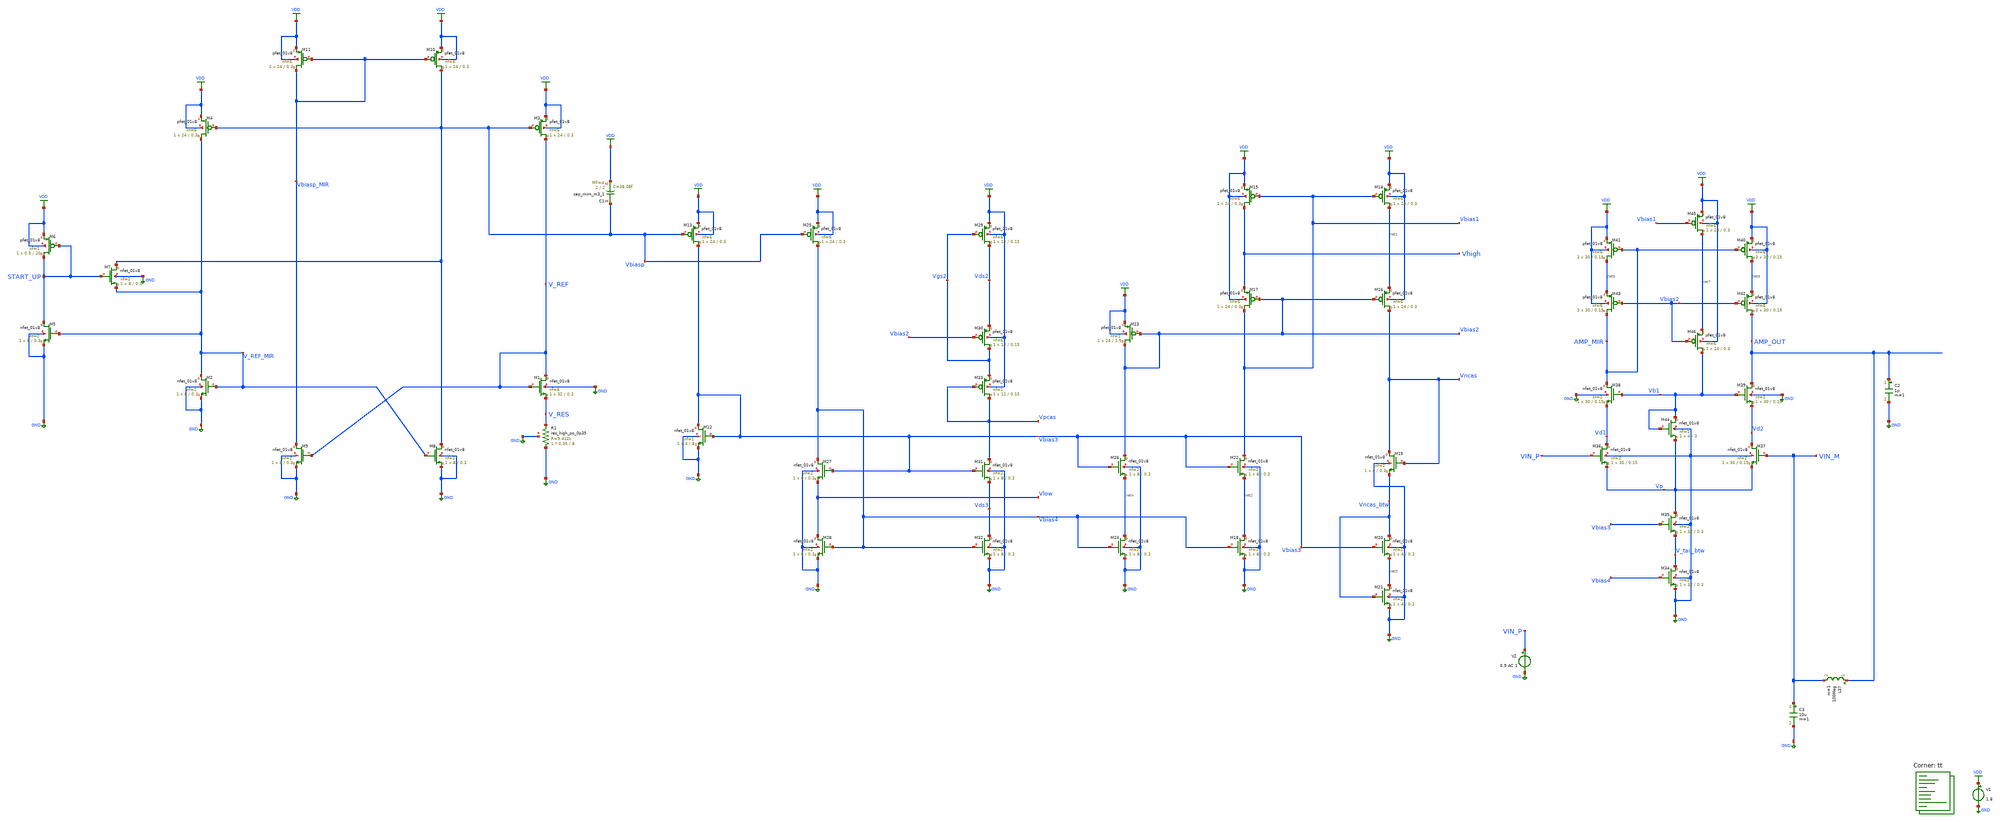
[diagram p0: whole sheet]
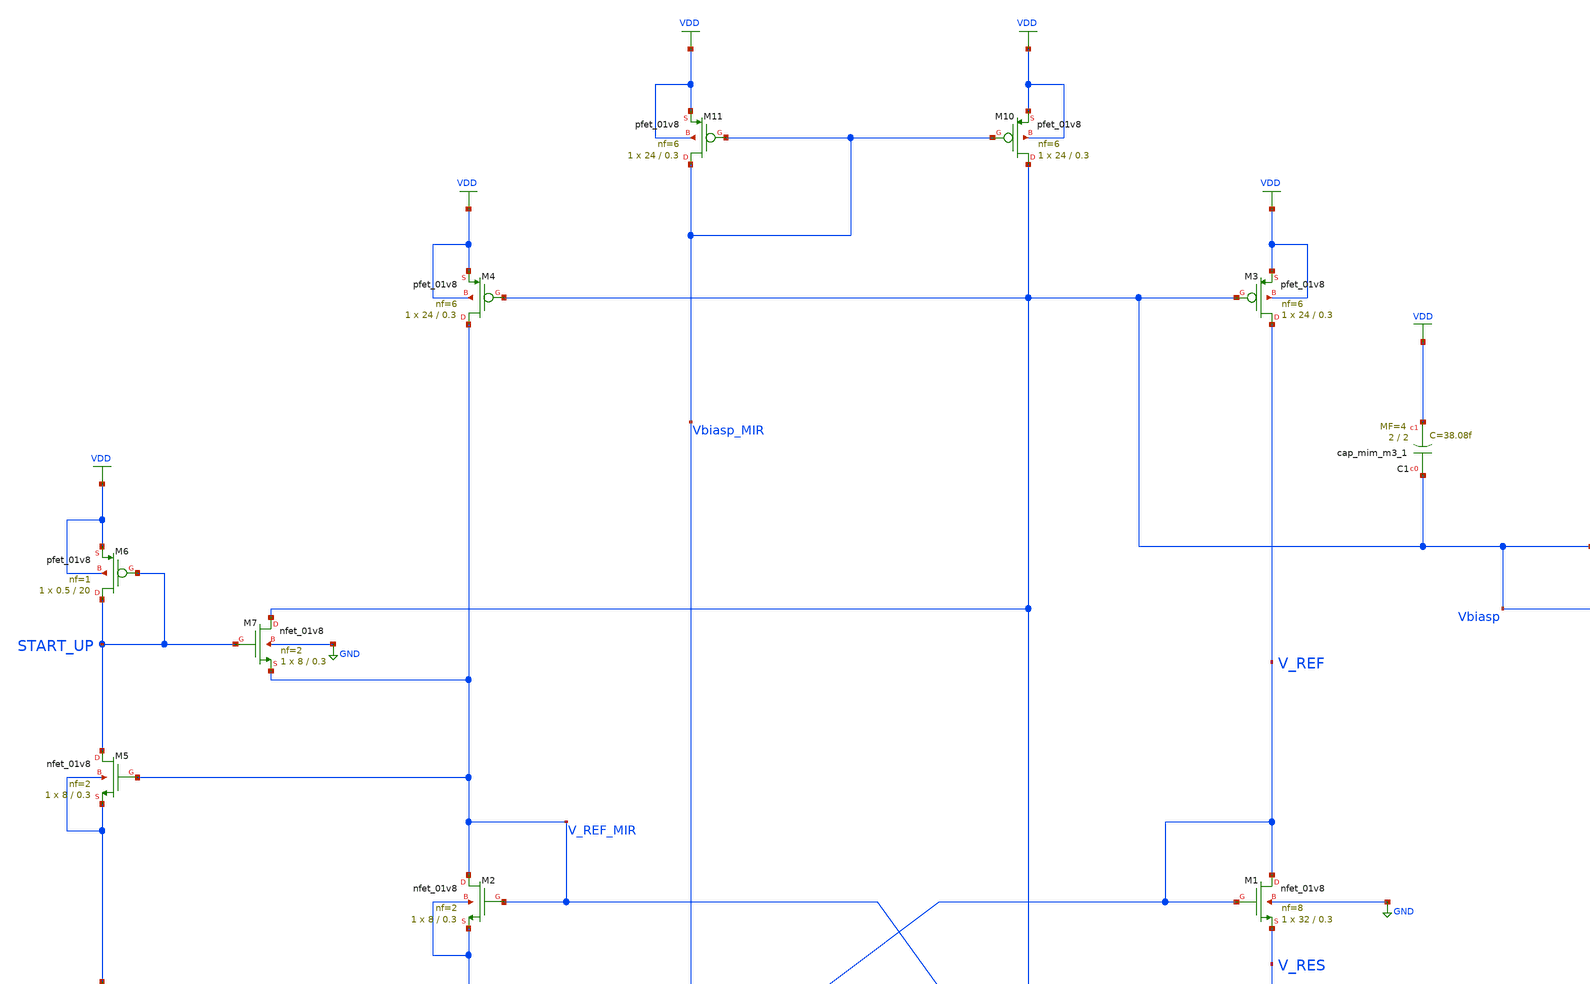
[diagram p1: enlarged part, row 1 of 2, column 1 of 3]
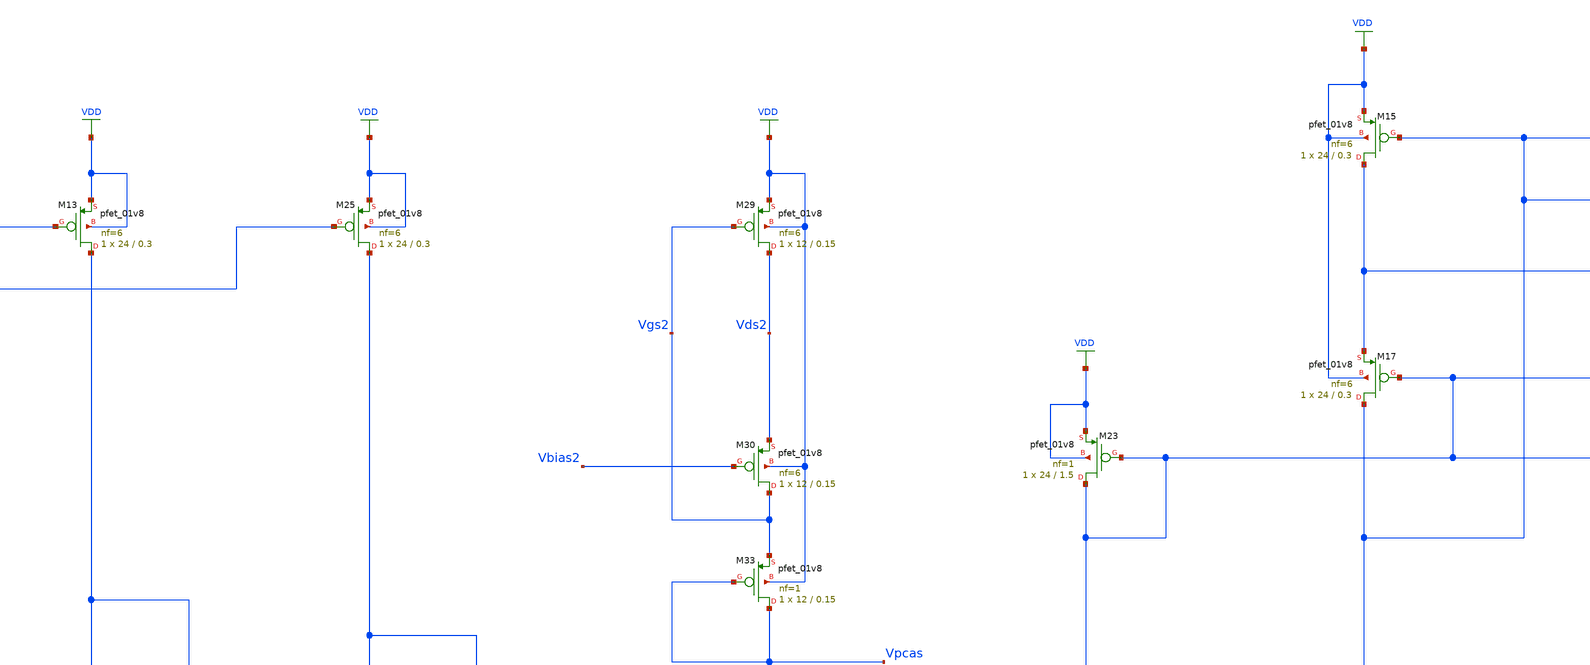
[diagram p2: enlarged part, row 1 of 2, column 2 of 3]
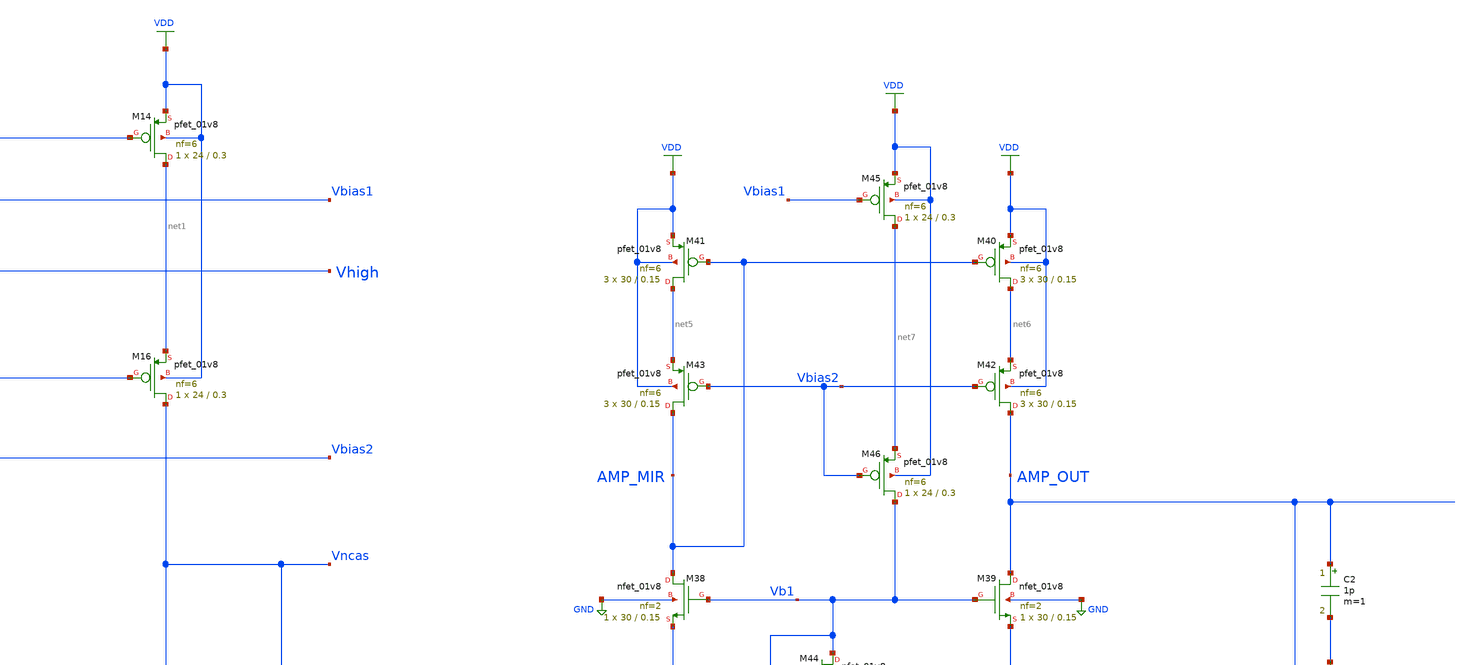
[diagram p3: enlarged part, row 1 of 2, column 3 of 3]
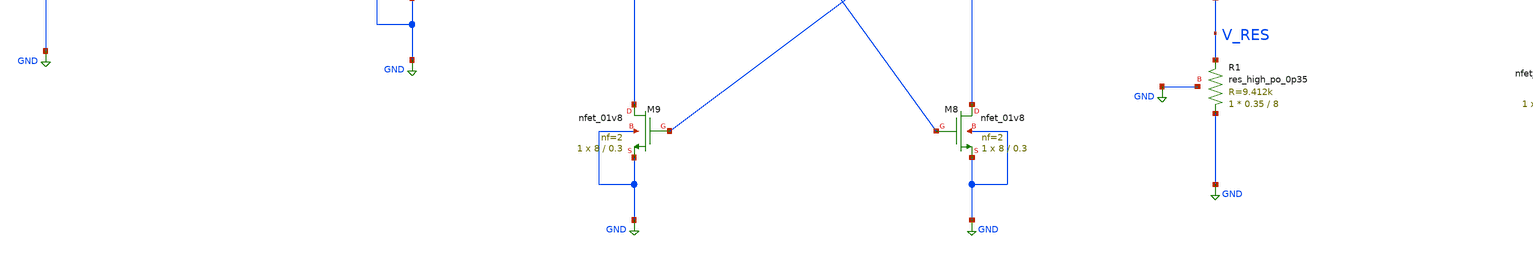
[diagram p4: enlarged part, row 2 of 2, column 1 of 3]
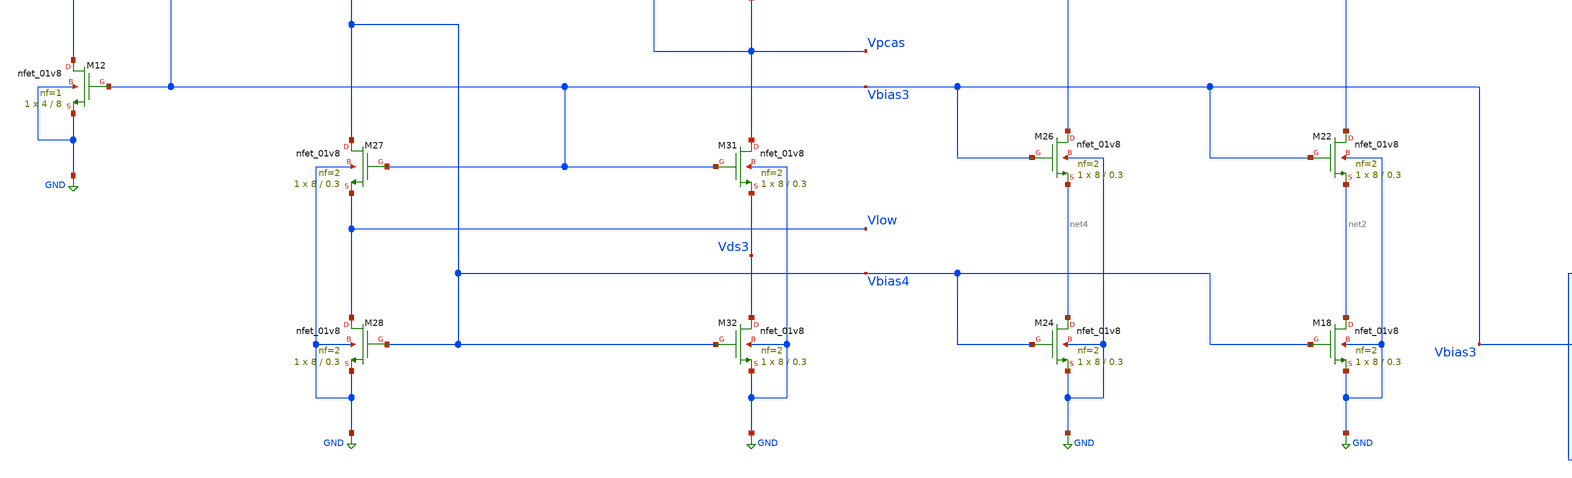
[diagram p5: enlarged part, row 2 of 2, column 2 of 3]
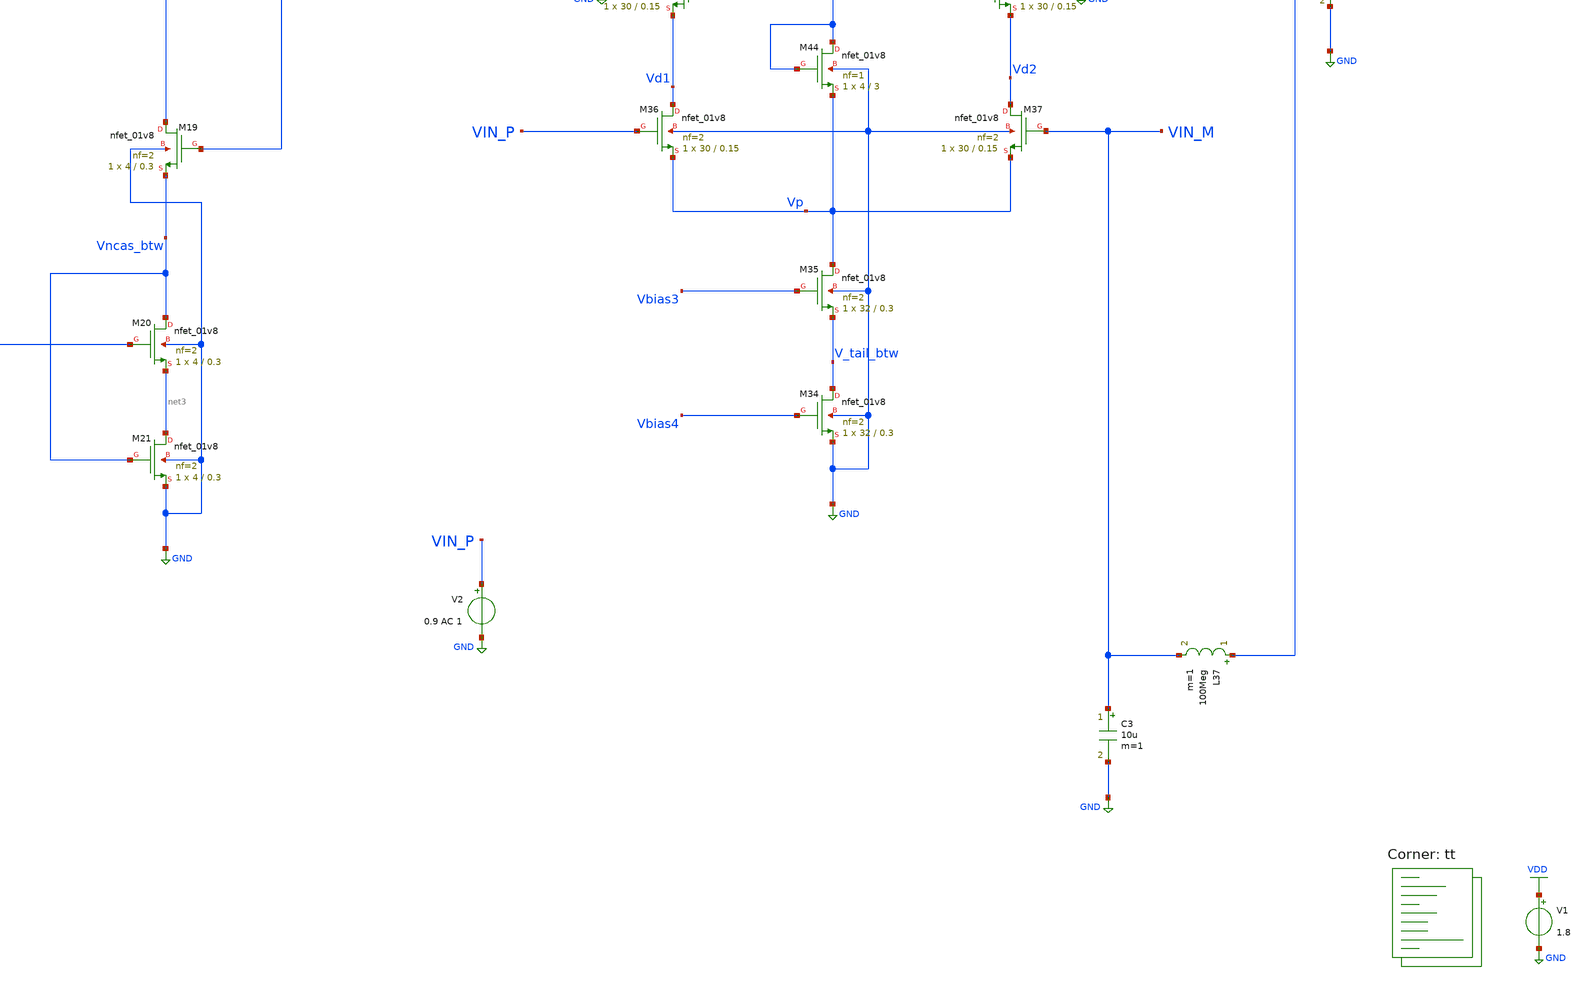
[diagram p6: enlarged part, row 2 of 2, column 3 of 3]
** sch_path: projects/ASU/EEE572/schematic/tb_tele_casc_diff_amp_AC.sch
**.subckt tb_tele_casc_diff_amp_AC
V1 VDD GND 1.8
XM1 V_REF V_REF V_RES GND sky130_fd_pr__nfet_01v8 L=0.3 W=32 nf=8 ad='int((nf+1)/2) * W/nf * 0.29' as='int((nf+2)/2) * W/nf * 0.29'
+ pd='2*int((nf+1)/2) * (W/nf + 0.29)' ps='2*int((nf+2)/2) * (W/nf + 0.29)' nrd='0.29 / W' nrs='0.29 / W'
+ sa=0 sb=0 sd=0 mult=1 m=1
XM2 V_REF_MIR V_REF_MIR GND GND sky130_fd_pr__nfet_01v8 L=0.3 W=8 nf=2 ad='int((nf+1)/2) * W/nf * 0.29'
+ as='int((nf+2)/2) * W/nf * 0.29' pd='2*int((nf+1)/2) * (W/nf + 0.29)' ps='2*int((nf+2)/2) * (W/nf + 0.29)'
+ nrd='0.29 / W' nrs='0.29 / W' sa=0 sb=0 sd=0 mult=1 m=1
XM5 START_UP V_REF_MIR GND GND sky130_fd_pr__nfet_01v8 L=0.3 W=8 nf=2 ad='int((nf+1)/2) * W/nf * 0.29'
+ as='int((nf+2)/2) * W/nf * 0.29' pd='2*int((nf+1)/2) * (W/nf + 0.29)' ps='2*int((nf+2)/2) * (W/nf + 0.29)'
+ nrd='0.29 / W' nrs='0.29 / W' sa=0 sb=0 sd=0 mult=1 m=1
XM7 Vbiasp START_UP V_REF_MIR GND sky130_fd_pr__nfet_01v8 L=0.3 W=8 nf=2 ad='int((nf+1)/2) * W/nf * 0.29'
+ as='int((nf+2)/2) * W/nf * 0.29' pd='2*int((nf+1)/2) * (W/nf + 0.29)' ps='2*int((nf+2)/2) * (W/nf + 0.29)'
+ nrd='0.29 / W' nrs='0.29 / W' sa=0 sb=0 sd=0 mult=1 m=1
XM6 START_UP START_UP VDD VDD sky130_fd_pr__pfet_01v8 L=20 W=0.5 nf=1 ad='int((nf+1)/2) * W/nf * 0.29'
+ as='int((nf+2)/2) * W/nf * 0.29' pd='2*int((nf+1)/2) * (W/nf + 0.29)' ps='2*int((nf+2)/2) * (W/nf + 0.29)'
+ nrd='0.29 / W' nrs='0.29 / W' sa=0 sb=0 sd=0 mult=1 m=1
XM3 V_REF Vbiasp VDD VDD sky130_fd_pr__pfet_01v8 L=0.3 W=24 nf=6 ad='int((nf+1)/2) * W/nf * 0.29' as='int((nf+2)/2) * W/nf * 0.29'
+ pd='2*int((nf+1)/2) * (W/nf + 0.29)' ps='2*int((nf+2)/2) * (W/nf + 0.29)' nrd='0.29 / W' nrs='0.29 / W'
+ sa=0 sb=0 sd=0 mult=1 m=1
XM4 V_REF_MIR Vbiasp VDD VDD sky130_fd_pr__pfet_01v8 L=0.3 W=24 nf=6 ad='int((nf+1)/2) * W/nf * 0.29'
+ as='int((nf+2)/2) * W/nf * 0.29' pd='2*int((nf+1)/2) * (W/nf + 0.29)' ps='2*int((nf+2)/2) * (W/nf + 0.29)'
+ nrd='0.29 / W' nrs='0.29 / W' sa=0 sb=0 sd=0 mult=1 m=1
XM8 Vbiasp V_REF_MIR GND GND sky130_fd_pr__nfet_01v8 L=0.3 W=8 nf=2 ad='int((nf+1)/2) * W/nf * 0.29'
+ as='int((nf+2)/2) * W/nf * 0.29' pd='2*int((nf+1)/2) * (W/nf + 0.29)' ps='2*int((nf+2)/2) * (W/nf + 0.29)'
+ nrd='0.29 / W' nrs='0.29 / W' sa=0 sb=0 sd=0 mult=1 m=1
XM9 Vbiasp_MIR V_REF GND GND sky130_fd_pr__nfet_01v8 L=0.3 W=8 nf=2 ad='int((nf+1)/2) * W/nf * 0.29'
+ as='int((nf+2)/2) * W/nf * 0.29' pd='2*int((nf+1)/2) * (W/nf + 0.29)' ps='2*int((nf+2)/2) * (W/nf + 0.29)'
+ nrd='0.29 / W' nrs='0.29 / W' sa=0 sb=0 sd=0 mult=1 m=1
XM10 Vbiasp Vbiasp_MIR VDD VDD sky130_fd_pr__pfet_01v8 L=0.3 W=24 nf=6 ad='int((nf+1)/2) * W/nf * 0.29'
+ as='int((nf+2)/2) * W/nf * 0.29' pd='2*int((nf+1)/2) * (W/nf + 0.29)' ps='2*int((nf+2)/2) * (W/nf + 0.29)'
+ nrd='0.29 / W' nrs='0.29 / W' sa=0 sb=0 sd=0 mult=1 m=1
XM11 Vbiasp_MIR Vbiasp_MIR VDD VDD sky130_fd_pr__pfet_01v8 L=0.3 W=24 nf=6 ad='int((nf+1)/2) * W/nf * 0.29'
+ as='int((nf+2)/2) * W/nf * 0.29' pd='2*int((nf+1)/2) * (W/nf + 0.29)' ps='2*int((nf+2)/2) * (W/nf + 0.29)'
+ nrd='0.29 / W' nrs='0.29 / W' sa=0 sb=0 sd=0 mult=1 m=1
XM12 Vbias3 Vbias3 GND GND sky130_fd_pr__nfet_01v8 L=8 W=4 nf=1 ad='int((nf+1)/2) * W/nf * 0.29' as='int((nf+2)/2) * W/nf * 0.29'
+ pd='2*int((nf+1)/2) * (W/nf + 0.29)' ps='2*int((nf+2)/2) * (W/nf + 0.29)' nrd='0.29 / W' nrs='0.29 / W'
+ sa=0 sb=0 sd=0 mult=1 m=1
XM13 Vbias3 Vbiasp VDD VDD sky130_fd_pr__pfet_01v8 L=0.3 W=24 nf=6 ad='int((nf+1)/2) * W/nf * 0.29' as='int((nf+2)/2) * W/nf * 0.29'
+ pd='2*int((nf+1)/2) * (W/nf + 0.29)' ps='2*int((nf+2)/2) * (W/nf + 0.29)' nrd='0.29 / W' nrs='0.29 / W'
+ sa=0 sb=0 sd=0 mult=1 m=1
XM14 net1 Vbias1 VDD VDD sky130_fd_pr__pfet_01v8 L=0.3 W=24 nf=6 ad='int((nf+1)/2) * W/nf * 0.29' as='int((nf+2)/2) * W/nf * 0.29'
+ pd='2*int((nf+1)/2) * (W/nf + 0.29)' ps='2*int((nf+2)/2) * (W/nf + 0.29)' nrd='0.29 / W' nrs='0.29 / W'
+ sa=0 sb=0 sd=0 mult=1 m=1
XM15 Vhigh Vbias1 VDD VDD sky130_fd_pr__pfet_01v8 L=0.3 W=24 nf=6 ad='int((nf+1)/2) * W/nf * 0.29' as='int((nf+2)/2) * W/nf * 0.29'
+ pd='2*int((nf+1)/2) * (W/nf + 0.29)' ps='2*int((nf+2)/2) * (W/nf + 0.29)' nrd='0.29 / W' nrs='0.29 / W'
+ sa=0 sb=0 sd=0 mult=1 m=1
XM16 Vncas Vbias2 net1 VDD sky130_fd_pr__pfet_01v8 L=0.3 W=24 nf=6 ad='int((nf+1)/2) * W/nf * 0.29' as='int((nf+2)/2) * W/nf * 0.29'
+ pd='2*int((nf+1)/2) * (W/nf + 0.29)' ps='2*int((nf+2)/2) * (W/nf + 0.29)' nrd='0.29 / W' nrs='0.29 / W'
+ sa=0 sb=0 sd=0 mult=1 m=1
XM17 Vbias1 Vbias2 Vhigh VDD sky130_fd_pr__pfet_01v8 L=0.3 W=24 nf=6 ad='int((nf+1)/2) * W/nf * 0.29'
+ as='int((nf+2)/2) * W/nf * 0.29' pd='2*int((nf+1)/2) * (W/nf + 0.29)' ps='2*int((nf+2)/2) * (W/nf + 0.29)'
+ nrd='0.29 / W' nrs='0.29 / W' sa=0 sb=0 sd=0 mult=1 m=1
XM18 net2 Vbias4 GND GND sky130_fd_pr__nfet_01v8 L=0.3 W=8 nf=2 ad='int((nf+1)/2) * W/nf * 0.29' as='int((nf+2)/2) * W/nf * 0.29'
+ pd='2*int((nf+1)/2) * (W/nf + 0.29)' ps='2*int((nf+2)/2) * (W/nf + 0.29)' nrd='0.29 / W' nrs='0.29 / W'
+ sa=0 sb=0 sd=0 mult=1 m=1
XM19 Vncas Vncas Vncas_btw GND sky130_fd_pr__nfet_01v8 L=0.3 W=4 nf=2 ad='int((nf+1)/2) * W/nf * 0.29'
+ as='int((nf+2)/2) * W/nf * 0.29' pd='2*int((nf+1)/2) * (W/nf + 0.29)' ps='2*int((nf+2)/2) * (W/nf + 0.29)'
+ nrd='0.29 / W' nrs='0.29 / W' sa=0 sb=0 sd=0 mult=1 m=1
XM20 Vncas_btw Vbias3 net3 GND sky130_fd_pr__nfet_01v8 L=0.3 W=4 nf=2 ad='int((nf+1)/2) * W/nf * 0.29'
+ as='int((nf+2)/2) * W/nf * 0.29' pd='2*int((nf+1)/2) * (W/nf + 0.29)' ps='2*int((nf+2)/2) * (W/nf + 0.29)'
+ nrd='0.29 / W' nrs='0.29 / W' sa=0 sb=0 sd=0 mult=1 m=1
XM21 net3 Vncas_btw GND GND sky130_fd_pr__nfet_01v8 L=0.3 W=4 nf=2 ad='int((nf+1)/2) * W/nf * 0.29' as='int((nf+2)/2) * W/nf * 0.29'
+ pd='2*int((nf+1)/2) * (W/nf + 0.29)' ps='2*int((nf+2)/2) * (W/nf + 0.29)' nrd='0.29 / W' nrs='0.29 / W'
+ sa=0 sb=0 sd=0 mult=1 m=1
XM25 Vbias4 Vbiasp VDD VDD sky130_fd_pr__pfet_01v8 L=0.3 W=24 nf=6 ad='int((nf+1)/2) * W/nf * 0.29' as='int((nf+2)/2) * W/nf * 0.29'
+ pd='2*int((nf+1)/2) * (W/nf + 0.29)' ps='2*int((nf+2)/2) * (W/nf + 0.29)' nrd='0.29 / W' nrs='0.29 / W'
+ sa=0 sb=0 sd=0 mult=1 m=1
XM27 Vbias4 Vbias3 Vlow GND sky130_fd_pr__nfet_01v8 L=0.3 W=8 nf=2 ad='int((nf+1)/2) * W/nf * 0.29' as='int((nf+2)/2) * W/nf * 0.29'
+ pd='2*int((nf+1)/2) * (W/nf + 0.29)' ps='2*int((nf+2)/2) * (W/nf + 0.29)' nrd='0.29 / W' nrs='0.29 / W'
+ sa=0 sb=0 sd=0 mult=1 m=1
XM28 Vlow Vbias4 GND GND sky130_fd_pr__nfet_01v8 L=0.3 W=8 nf=2 ad='int((nf+1)/2) * W/nf * 0.29' as='int((nf+2)/2) * W/nf * 0.29'
+ pd='2*int((nf+1)/2) * (W/nf + 0.29)' ps='2*int((nf+2)/2) * (W/nf + 0.29)' nrd='0.29 / W' nrs='0.29 / W'
+ sa=0 sb=0 sd=0 mult=1 m=1
XM29 Vds2 Vgs2 VDD VDD sky130_fd_pr__pfet_01v8 L=0.15 W=12 nf=6 ad='int((nf+1)/2) * W/nf * 0.29' as='int((nf+2)/2) * W/nf * 0.29'
+ pd='2*int((nf+1)/2) * (W/nf + 0.29)' ps='2*int((nf+2)/2) * (W/nf + 0.29)' nrd='0.29 / W' nrs='0.29 / W'
+ sa=0 sb=0 sd=0 mult=1 m=1
XM30 Vgs2 Vbias2 Vds2 VDD sky130_fd_pr__pfet_01v8 L=0.15 W=12 nf=6 ad='int((nf+1)/2) * W/nf * 0.29' as='int((nf+2)/2) * W/nf * 0.29'
+ pd='2*int((nf+1)/2) * (W/nf + 0.29)' ps='2*int((nf+2)/2) * (W/nf + 0.29)' nrd='0.29 / W' nrs='0.29 / W'
+ sa=0 sb=0 sd=0 mult=1 m=1
XM31 Vpcas Vbias3 Vds3 GND sky130_fd_pr__nfet_01v8 L=0.3 W=8 nf=2 ad='int((nf+1)/2) * W/nf * 0.29' as='int((nf+2)/2) * W/nf * 0.29'
+ pd='2*int((nf+1)/2) * (W/nf + 0.29)' ps='2*int((nf+2)/2) * (W/nf + 0.29)' nrd='0.29 / W' nrs='0.29 / W'
+ sa=0 sb=0 sd=0 mult=1 m=1
XM32 Vds3 Vbias4 GND GND sky130_fd_pr__nfet_01v8 L=0.3 W=8 nf=2 ad='int((nf+1)/2) * W/nf * 0.29' as='int((nf+2)/2) * W/nf * 0.29'
+ pd='2*int((nf+1)/2) * (W/nf + 0.29)' ps='2*int((nf+2)/2) * (W/nf + 0.29)' nrd='0.29 / W' nrs='0.29 / W'
+ sa=0 sb=0 sd=0 mult=1 m=1
XM33 Vpcas Vpcas Vgs2 VDD sky130_fd_pr__pfet_01v8 L=0.15 W=12 nf=1 ad='int((nf+1)/2) * W/nf * 0.29' as='int((nf+2)/2) * W/nf * 0.29'
+ pd='2*int((nf+1)/2) * (W/nf + 0.29)' ps='2*int((nf+2)/2) * (W/nf + 0.29)' nrd='0.29 / W' nrs='0.29 / W'
+ sa=0 sb=0 sd=0 mult=1 m=1
XM22 Vbias1 Vbias3 net2 GND sky130_fd_pr__nfet_01v8 L=0.3 W=8 nf=2 ad='int((nf+1)/2) * W/nf * 0.29' as='int((nf+2)/2) * W/nf * 0.29'
+ pd='2*int((nf+1)/2) * (W/nf + 0.29)' ps='2*int((nf+2)/2) * (W/nf + 0.29)' nrd='0.29 / W' nrs='0.29 / W'
+ sa=0 sb=0 sd=0 mult=1 m=1
XM23 Vbias2 Vbias2 VDD VDD sky130_fd_pr__pfet_01v8 L=1.5 W=24 nf=1 ad='int((nf+1)/2) * W/nf * 0.29' as='int((nf+2)/2) * W/nf * 0.29'
+ pd='2*int((nf+1)/2) * (W/nf + 0.29)' ps='2*int((nf+2)/2) * (W/nf + 0.29)' nrd='0.29 / W' nrs='0.29 / W'
+ sa=0 sb=0 sd=0 mult=1 m=1
XM24 net4 Vbias4 GND GND sky130_fd_pr__nfet_01v8 L=0.3 W=8 nf=2 ad='int((nf+1)/2) * W/nf * 0.29' as='int((nf+2)/2) * W/nf * 0.29'
+ pd='2*int((nf+1)/2) * (W/nf + 0.29)' ps='2*int((nf+2)/2) * (W/nf + 0.29)' nrd='0.29 / W' nrs='0.29 / W'
+ sa=0 sb=0 sd=0 mult=1 m=1
XM26 Vbias2 Vbias3 net4 GND sky130_fd_pr__nfet_01v8 L=0.3 W=8 nf=2 ad='int((nf+1)/2) * W/nf * 0.29' as='int((nf+2)/2) * W/nf * 0.29'
+ pd='2*int((nf+1)/2) * (W/nf + 0.29)' ps='2*int((nf+2)/2) * (W/nf + 0.29)' nrd='0.29 / W' nrs='0.29 / W'
+ sa=0 sb=0 sd=0 mult=1 m=1
XC1 Vbiasp VDD sky130_fd_pr__cap_mim_m3_1 W=2 L=2 MF=4 m=4
XM34 V_tail_btw Vbias4 GND GND sky130_fd_pr__nfet_01v8 L=0.3 W=32 nf=2 ad='int((nf+1)/2) * W/nf * 0.29'
+ as='int((nf+2)/2) * W/nf * 0.29' pd='2*int((nf+1)/2) * (W/nf + 0.29)' ps='2*int((nf+2)/2) * (W/nf + 0.29)'
+ nrd='0.29 / W' nrs='0.29 / W' sa=0 sb=0 sd=0 mult=1 m=1
XM35 Vp Vbias3 V_tail_btw GND sky130_fd_pr__nfet_01v8 L=0.3 W=32 nf=2 ad='int((nf+1)/2) * W/nf * 0.29'
+ as='int((nf+2)/2) * W/nf * 0.29' pd='2*int((nf+1)/2) * (W/nf + 0.29)' ps='2*int((nf+2)/2) * (W/nf + 0.29)'
+ nrd='0.29 / W' nrs='0.29 / W' sa=0 sb=0 sd=0 mult=1 m=1
XM36 Vd1 VIN_P Vp GND sky130_fd_pr__nfet_01v8 L=0.15 W=30 nf=2 ad='int((nf+1)/2) * W/nf * 0.29' as='int((nf+2)/2) * W/nf * 0.29'
+ pd='2*int((nf+1)/2) * (W/nf + 0.29)' ps='2*int((nf+2)/2) * (W/nf + 0.29)' nrd='0.29 / W' nrs='0.29 / W'
+ sa=0 sb=0 sd=0 mult=1 m=1
XM37 Vd2 VIN_M Vp GND sky130_fd_pr__nfet_01v8 L=0.15 W=30 nf=2 ad='int((nf+1)/2) * W/nf * 0.29' as='int((nf+2)/2) * W/nf * 0.29'
+ pd='2*int((nf+1)/2) * (W/nf + 0.29)' ps='2*int((nf+2)/2) * (W/nf + 0.29)' nrd='0.29 / W' nrs='0.29 / W'
+ sa=0 sb=0 sd=0 mult=1 m=1
XM38 AMP_MIR Vb1 Vd1 GND sky130_fd_pr__nfet_01v8 L=0.15 W=30 nf=2 ad='int((nf+1)/2) * W/nf * 0.29' as='int((nf+2)/2) * W/nf * 0.29'
+ pd='2*int((nf+1)/2) * (W/nf + 0.29)' ps='2*int((nf+2)/2) * (W/nf + 0.29)' nrd='0.29 / W' nrs='0.29 / W'
+ sa=0 sb=0 sd=0 mult=1 m=1
XM39 AMP_OUT Vb1 Vd2 GND sky130_fd_pr__nfet_01v8 L=0.15 W=30 nf=2 ad='int((nf+1)/2) * W/nf * 0.29' as='int((nf+2)/2) * W/nf * 0.29'
+ pd='2*int((nf+1)/2) * (W/nf + 0.29)' ps='2*int((nf+2)/2) * (W/nf + 0.29)' nrd='0.29 / W' nrs='0.29 / W'
+ sa=0 sb=0 sd=0 mult=1 m=1
XM40 net6 AMP_MIR VDD VDD sky130_fd_pr__pfet_01v8 L=0.15 W=30 nf=6 ad='int((nf+1)/2) * W/nf * 0.29' as='int((nf+2)/2) * W/nf * 0.29'
+ pd='2*int((nf+1)/2) * (W/nf + 0.29)' ps='2*int((nf+2)/2) * (W/nf + 0.29)' nrd='0.29 / W' nrs='0.29 / W'
+ sa=0 sb=0 sd=0 mult=3 m=3
XM41 net5 AMP_MIR VDD VDD sky130_fd_pr__pfet_01v8 L=0.15 W=30 nf=6 ad='int((nf+1)/2) * W/nf * 0.29' as='int((nf+2)/2) * W/nf * 0.29'
+ pd='2*int((nf+1)/2) * (W/nf + 0.29)' ps='2*int((nf+2)/2) * (W/nf + 0.29)' nrd='0.29 / W' nrs='0.29 / W'
+ sa=0 sb=0 sd=0 mult=3 m=3
XM42 AMP_OUT Vbias2 net6 VDD sky130_fd_pr__pfet_01v8 L=0.15 W=30 nf=6 ad='int((nf+1)/2) * W/nf * 0.29'
+ as='int((nf+2)/2) * W/nf * 0.29' pd='2*int((nf+1)/2) * (W/nf + 0.29)' ps='2*int((nf+2)/2) * (W/nf + 0.29)'
+ nrd='0.29 / W' nrs='0.29 / W' sa=0 sb=0 sd=0 mult=3 m=3
XM43 AMP_MIR Vbias2 net5 VDD sky130_fd_pr__pfet_01v8 L=0.15 W=30 nf=6 ad='int((nf+1)/2) * W/nf * 0.29'
+ as='int((nf+2)/2) * W/nf * 0.29' pd='2*int((nf+1)/2) * (W/nf + 0.29)' ps='2*int((nf+2)/2) * (W/nf + 0.29)'
+ nrd='0.29 / W' nrs='0.29 / W' sa=0 sb=0 sd=0 mult=3 m=3
XM44 Vb1 Vb1 Vp GND sky130_fd_pr__nfet_01v8 L=3 W=4 nf=1 ad='int((nf+1)/2) * W/nf * 0.29' as='int((nf+2)/2) * W/nf * 0.29'
+ pd='2*int((nf+1)/2) * (W/nf + 0.29)' ps='2*int((nf+2)/2) * (W/nf + 0.29)' nrd='0.29 / W' nrs='0.29 / W'
+ sa=0 sb=0 sd=0 mult=1 m=1
XM45 net7 Vbias1 VDD VDD sky130_fd_pr__pfet_01v8 L=0.3 W=24 nf=6 ad='int((nf+1)/2) * W/nf * 0.29' as='int((nf+2)/2) * W/nf * 0.29'
+ pd='2*int((nf+1)/2) * (W/nf + 0.29)' ps='2*int((nf+2)/2) * (W/nf + 0.29)' nrd='0.29 / W' nrs='0.29 / W'
+ sa=0 sb=0 sd=0 mult=1 m=1
XM46 Vb1 Vbias2 net7 VDD sky130_fd_pr__pfet_01v8 L=0.3 W=24 nf=6 ad='int((nf+1)/2) * W/nf * 0.29' as='int((nf+2)/2) * W/nf * 0.29'
+ pd='2*int((nf+1)/2) * (W/nf + 0.29)' ps='2*int((nf+2)/2) * (W/nf + 0.29)' nrd='0.29 / W' nrs='0.29 / W'
+ sa=0 sb=0 sd=0 mult=1 m=1
V2 VIN_P GND 0.9 AC 1
XR1 GND V_RES GND sky130_fd_pr__res_high_po_0p35 L=8 mult=1 m=1
C2 AMP_OUT GND 1p m=1
C3 VIN_M GND 10u m=1
L37 AMP_OUT VIN_M 100Meg m=1
**** begin user architecture code
.lib $::SKYWATER_MODELS/sky130.lib.spice tt



.options method=gear
.options wnflag=1
.options savecurrents

.save @m.xm34.msky130_fd_pr__nfet_01v8[gm] @m.xm34.msky130_fd_pr__nfet_01v8[vth] @m.xm35.msky130_fd_pr__nfet_01v8[gm] @m.xm35.msky130_fd_pr__nfet_01v8[vth] @m.xm36.msky130_fd_pr__nfet_01v8[gm] @m.xm36.msky130_fd_pr__nfet_01v8[vth] @m.xm37.msky130_fd_pr__nfet_01v8[gm] @m.xm37.msky130_fd_pr__nfet_01v8[vth] @m.xm44.msky130_fd_pr__nfet_01v8[gm] @m.xm44.msky130_fd_pr__nfet_01v8[vth] @m.xm38.msky130_fd_pr__nfet_01v8[gm] @m.xm38.msky130_fd_pr__nfet_01v8[vth] @m.xm39.msky130_fd_pr__nfet_01v8[gm] @m.xm39.msky130_fd_pr__nfet_01v8[vth] @m.xm43.msky130_fd_pr__pfet_01v8[gm] @m.xm43.msky130_fd_pr__pfet_01v8[vth] @m.xm42.msky130_fd_pr__pfet_01v8[gm] @m.xm42.msky130_fd_pr__pfet_01v8[vth] @m.xm46.msky130_fd_pr__pfet_01v8[gm] @m.xm46.msky130_fd_pr__pfet_01v8[vth] @m.xm41.msky130_fd_pr__pfet_01v8[gm] @m.xm41.msky130_fd_pr__pfet_01v8[vth] @m.xm40.msky130_fd_pr__pfet_01v8[gm] @m.xm40.msky130_fd_pr__pfet_01v8[vth] @m.xm45.msky130_fd_pr__pfet_01v8[gm] @m.xm45.msky130_fd_pr__pfet_01v8[vth] @m.xm29.msky130_fd_pr__pfet_01v8[gm] @m.xm29.msky130_fd_pr__pfet_01v8[vth] @m.xm30.msky130_fd_pr__pfet_01v8[gm] @m.xm30.msky130_fd_pr__pfet_01v8[vth] @m.xm31.msky130_fd_pr__nfet_01v8[gm] @m.xm31.msky130_fd_pr__nfet_01v8[vth] @m.xm32.msky130_fd_pr__nfet_01v8[gm] @m.xm32.msky130_fd_pr__nfet_01v8[vth] @m.xm15.msky130_fd_pr__pfet_01v8[gm] @m.xm15.msky130_fd_pr__pfet_01v8[vth] @m.xm14.msky130_fd_pr__pfet_01v8[gm] @m.xm14.msky130_fd_pr__pfet_01v8[vth] @m.xm17.msky130_fd_pr__pfet_01v8[gm] @m.xm17.msky130_fd_pr__pfet_01v8[vth] @m.xm16.msky130_fd_pr__pfet_01v8[gm] @m.xm16.msky130_fd_pr__pfet_01v8[vth] @m.xm27.msky130_fd_pr__nfet_01v8[gm] @m.xm27.msky130_fd_pr__nfet_01v8[vth] @m.xm28.msky130_fd_pr__nfet_01v8[gm] @m.xm28.msky130_fd_pr__nfet_01v8[vth] @m.xm19.msky130_fd_pr__nfet_01v8[gm] @m.xm19.msky130_fd_pr__nfet_01v8[vth] @m.xm20.msky130_fd_pr__nfet_01v8[gm] @m.xm20.msky130_fd_pr__nfet_01v8[vth] @m.xm21.msky130_fd_pr__nfet_01v8[gm] @m.xm21.msky130_fd_pr__nfet_01v8[vth] @m.xm33.msky130_fd_pr__pfet_01v8[gm] @m.xm33.msky130_fd_pr__pfet_01v8[vth] @m.xm22.msky130_fd_pr__nfet_01v8[gm] @m.xm22.msky130_fd_pr__nfet_01v8[vth] @m.xm26.msky130_fd_pr__nfet_01v8[gm] @m.xm26.msky130_fd_pr__nfet_01v8[vth] @m.xm24.msky130_fd_pr__nfet_01v8[gm] @m.xm24.msky130_fd_pr__nfet_01v8[vth] @m.xm18.msky130_fd_pr__nfet_01v8[gm] @m.xm18.msky130_fd_pr__nfet_01v8[vth]


.control

  save all
  * save v(amp_out) v(ph(amp_out)) v(VIN_P) v(VIN_M)
  * dc V1 0.0 2.0 0.005
  ac dec 10 1k 10G
  * ac dec 20 1 1T
  * op
  * tran 0.05ns 5us
  remzerovec
  write tb_tele_casc_diff_amp_AC.raw
  set appendwrite

.endc




**** end user architecture code
**.ends
.GLOBAL GND
.GLOBAL VDD
.end
